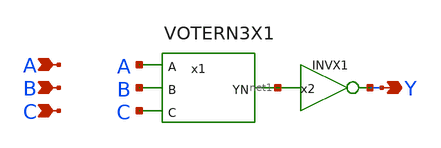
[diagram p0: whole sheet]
** sch_path: archives/lib/xschem/VOTER3X1.sch
**.subckt VOTER3X1 Y A B C
*.opin Y
*.ipin A
*.ipin B
*.ipin C
x1 A B C net1 VDD VSS VOTERN3X1
x2 Y net1 VDD VSS INVX1
**.ends
.end
